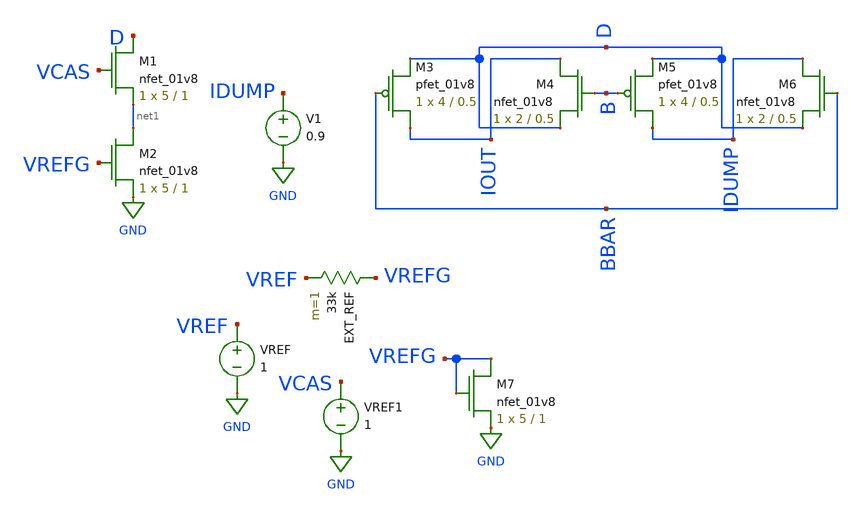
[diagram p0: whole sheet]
** sch_path: MP3/Schematics/bit_cell.sch
**.subckt bit_cell
XM1 D VCAS net1 GND sky130_fd_pr__nfet_01v8 L=1 W=5 nf=1 ad='int((nf+1)/2) * W/nf * 0.29' as='int((nf+2)/2) * W/nf * 0.29'
+ pd='2*int((nf+1)/2) * (W/nf + 0.29)' ps='2*int((nf+2)/2) * (W/nf + 0.29)' nrd='0.29 / W' nrs='0.29 / W'
+ sa=0 sb=0 sd=0 mult=1 m=1
XM2 net1 VREFG GND GND sky130_fd_pr__nfet_01v8 L=1 W=5 nf=1 ad='int((nf+1)/2) * W/nf * 0.29' as='int((nf+2)/2) * W/nf * 0.29'
+ pd='2*int((nf+1)/2) * (W/nf + 0.29)' ps='2*int((nf+2)/2) * (W/nf + 0.29)' nrd='0.29 / W' nrs='0.29 / W'
+ sa=0 sb=0 sd=0 mult=1 m=1
XM3 IOUT BBAR D VDD sky130_fd_pr__pfet_01v8 L=0.5 W=4 nf=1 ad='int((nf+1)/2) * W/nf * 0.29' as='int((nf+2)/2) * W/nf * 0.29'
+ pd='2*int((nf+1)/2) * (W/nf + 0.29)' ps='2*int((nf+2)/2) * (W/nf + 0.29)' nrd='0.29 / W' nrs='0.29 / W'
+ sa=0 sb=0 sd=0 mult=1 m=1
XM4 IOUT B D GND sky130_fd_pr__nfet_01v8 L=0.5 W=2 nf=1 ad='int((nf+1)/2) * W/nf * 0.29' as='int((nf+2)/2) * W/nf * 0.29'
+ pd='2*int((nf+1)/2) * (W/nf + 0.29)' ps='2*int((nf+2)/2) * (W/nf + 0.29)' nrd='0.29 / W' nrs='0.29 / W'
+ sa=0 sb=0 sd=0 mult=1 m=1
XM5 IDUMP B D VDD sky130_fd_pr__pfet_01v8 L=0.5 W=4 nf=1 ad='int((nf+1)/2) * W/nf * 0.29' as='int((nf+2)/2) * W/nf * 0.29'
+ pd='2*int((nf+1)/2) * (W/nf + 0.29)' ps='2*int((nf+2)/2) * (W/nf + 0.29)' nrd='0.29 / W' nrs='0.29 / W'
+ sa=0 sb=0 sd=0 mult=1 m=1
XM6 IDUMP BBAR D GND sky130_fd_pr__nfet_01v8 L=0.5 W=2 nf=1 ad='int((nf+1)/2) * W/nf * 0.29' as='int((nf+2)/2) * W/nf * 0.29'
+ pd='2*int((nf+1)/2) * (W/nf + 0.29)' ps='2*int((nf+2)/2) * (W/nf + 0.29)' nrd='0.29 / W' nrs='0.29 / W'
+ sa=0 sb=0 sd=0 mult=1 m=1
V1 IDUMP GND 0.9
XM7 VREFG VREFG GND GND sky130_fd_pr__nfet_01v8 L=1 W=5 nf=1 ad='int((nf+1)/2) * W/nf * 0.29' as='int((nf+2)/2) * W/nf * 0.29'
+ pd='2*int((nf+1)/2) * (W/nf + 0.29)' ps='2*int((nf+2)/2) * (W/nf + 0.29)' nrd='0.29 / W' nrs='0.29 / W'
+ sa=0 sb=0 sd=0 mult=1 m=1
EXT_REF VREFG VREF 33k m=1
VREF VREF GND 1
VREF1 VCAS GND 1
**.ends
.GLOBAL GND
.end
